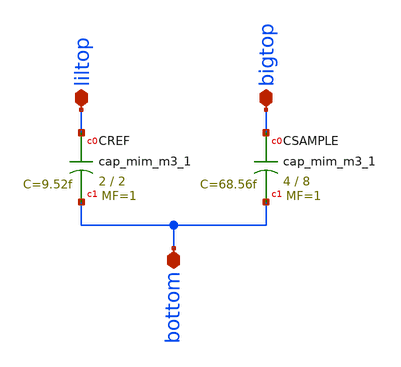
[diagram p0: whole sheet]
** sch_path: analog/xschem/mimcaps.sch
**.subckt mimcaps bottom liltop bigtop
*.iopin bottom
*.iopin liltop
*.iopin bigtop
XCSAMPLE bigtop bottom sky130_fd_pr__cap_mim_m3_1 W=4 L=8 MF=1 m=1
XCREF liltop bottom sky130_fd_pr__cap_mim_m3_1 W=2 L=2 MF=1 m=1
**.ends
.end
